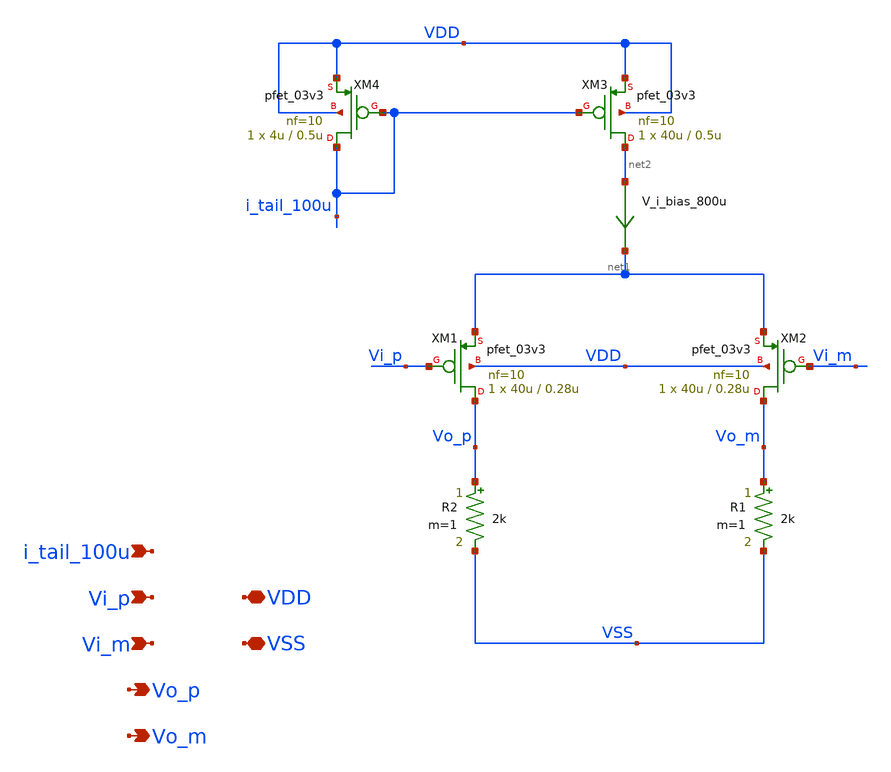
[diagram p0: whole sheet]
** sch_path: designs/output_amplifier/schematic/pmos_output_buffer.sch
**.subckt pmos_output_buffer VDD VSS Vi_p Vi_m Vo_p Vo_m i_tail_100u
*.iopin VDD
*.iopin VSS
*.ipin Vi_p
*.ipin Vi_m
*.opin Vo_p
*.opin Vo_m
*.ipin i_tail_100u
XM1 Vo_p Vi_p net1 VDD pfet_03v3 L=0.28u W=40u nf=10 ad='int((nf+1)/2) * W/nf * 0.18u' as='int((nf+2)/2) * W/nf * 0.18u'
+ pd='2*int((nf+1)/2) * (W/nf + 0.18u)' ps='2*int((nf+2)/2) * (W/nf + 0.18u)' nrd='0.18u / W' nrs='0.18u / W'
+ sa=0 sb=0 sd=0 m=1
XM2 Vo_m Vi_m net1 VDD pfet_03v3 L=0.28u W=40u nf=10 ad='int((nf+1)/2) * W/nf * 0.18u' as='int((nf+2)/2) * W/nf * 0.18u'
+ pd='2*int((nf+1)/2) * (W/nf + 0.18u)' ps='2*int((nf+2)/2) * (W/nf + 0.18u)' nrd='0.18u / W' nrs='0.18u / W'
+ sa=0 sb=0 sd=0 m=1
R1 Vo_m VSS 2k m=1
R2 Vo_p VSS 2k m=1
XM3 net2 i_tail_100u VDD VDD pfet_03v3 L=0.5u W=40u nf=10 ad='int((nf+1)/2) * W/nf * 0.18u' as='int((nf+2)/2) * W/nf * 0.18u'
+ pd='2*int((nf+1)/2) * (W/nf + 0.18u)' ps='2*int((nf+2)/2) * (W/nf + 0.18u)' nrd='0.18u / W' nrs='0.18u / W'
+ sa=0 sb=0 sd=0 m=1
XM4 i_tail_100u i_tail_100u VDD VDD pfet_03v3 L=0.5u W=4u nf=10 ad='int((nf+1)/2) * W/nf * 0.18u' as='int((nf+2)/2) * W/nf * 0.18u'
+ pd='2*int((nf+1)/2) * (W/nf + 0.18u)' ps='2*int((nf+2)/2) * (W/nf + 0.18u)' nrd='0.18u / W' nrs='0.18u / W'
+ sa=0 sb=0 sd=0 m=1
V_i_bias_800u net2 net1 0
.save i(v_i_bias_800u)
**.ends
.end
